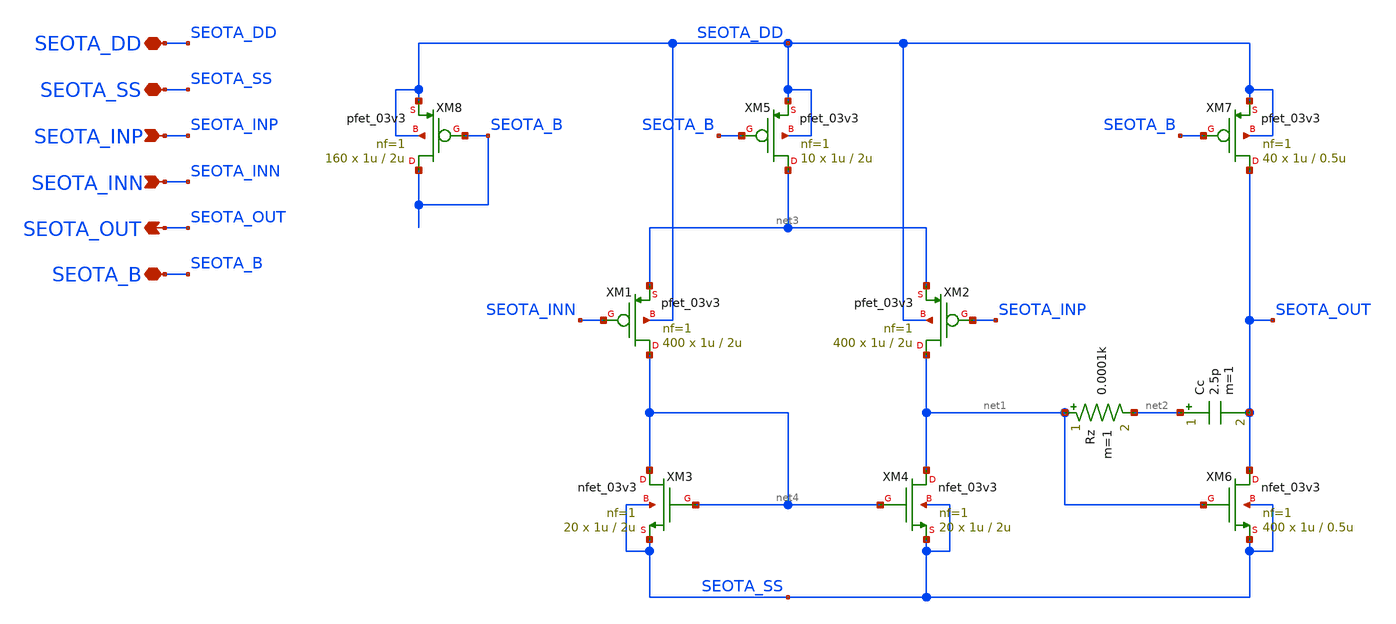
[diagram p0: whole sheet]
** sch_path: Design_Files/IC Design/Schematic/SE_OTA/SE_OTA_PMOS.sch
**.subckt SE_OTA_PMOS SEOTA_DD SEOTA_SS SEOTA_INP SEOTA_INN SEOTA_OUT SEOTA_B
*.iopin SEOTA_DD
*.iopin SEOTA_SS
*.ipin SEOTA_INP
*.ipin SEOTA_INN
*.opin SEOTA_OUT
*.iopin SEOTA_B
XM4 net1 net4 SEOTA_SS SEOTA_SS nfet_03v3 L=2u W=1u nf=1 ad='int((nf+1)/2) * W/nf * 0.18u' as='int((nf+2)/2) * W/nf * 0.18u'
+ pd='2*int((nf+1)/2) * (W/nf + 0.18u)' ps='2*int((nf+2)/2) * (W/nf + 0.18u)' nrd='0.18u / W' nrs='0.18u / W'
+ sa=0 sb=0 sd=0 m=20
XM3 net4 net4 SEOTA_SS SEOTA_SS nfet_03v3 L=2u W=1u nf=1 ad='int((nf+1)/2) * W/nf * 0.18u' as='int((nf+2)/2) * W/nf * 0.18u'
+ pd='2*int((nf+1)/2) * (W/nf + 0.18u)' ps='2*int((nf+2)/2) * (W/nf + 0.18u)' nrd='0.18u / W' nrs='0.18u / W'
+ sa=0 sb=0 sd=0 m=20
XM1 net4 SEOTA_INN net3 SEOTA_DD pfet_03v3 L=2u W=1u nf=1 ad='int((nf+1)/2) * W/nf * 0.18u' as='int((nf+2)/2) * W/nf * 0.18u'
+ pd='2*int((nf+1)/2) * (W/nf + 0.18u)' ps='2*int((nf+2)/2) * (W/nf + 0.18u)' nrd='0.18u / W' nrs='0.18u / W'
+ sa=0 sb=0 sd=0 m=400
XM2 net1 SEOTA_INP net3 SEOTA_DD pfet_03v3 L=2u W=1u nf=1 ad='int((nf+1)/2) * W/nf * 0.18u' as='int((nf+2)/2) * W/nf * 0.18u'
+ pd='2*int((nf+1)/2) * (W/nf + 0.18u)' ps='2*int((nf+2)/2) * (W/nf + 0.18u)' nrd='0.18u / W' nrs='0.18u / W'
+ sa=0 sb=0 sd=0 m=400
XM7 SEOTA_OUT SEOTA_B SEOTA_DD SEOTA_DD pfet_03v3 L=0.5u W=1u nf=1 ad='int((nf+1)/2) * W/nf * 0.18u'
+ as='int((nf+2)/2) * W/nf * 0.18u' pd='2*int((nf+1)/2) * (W/nf + 0.18u)' ps='2*int((nf+2)/2) * (W/nf + 0.18u)'
+ nrd='0.18u / W' nrs='0.18u / W' sa=0 sb=0 sd=0 m=40
Rz net1 net2 0.0001k m=1
XM5 net3 SEOTA_B SEOTA_DD SEOTA_DD pfet_03v3 L=2u W=1u nf=1 ad='int((nf+1)/2) * W/nf * 0.18u' as='int((nf+2)/2) * W/nf * 0.18u'
+ pd='2*int((nf+1)/2) * (W/nf + 0.18u)' ps='2*int((nf+2)/2) * (W/nf + 0.18u)' nrd='0.18u / W' nrs='0.18u / W'
+ sa=0 sb=0 sd=0 m=10
XM8 SEOTA_B SEOTA_B SEOTA_DD SEOTA_DD pfet_03v3 L=2u W=1u nf=1 ad='int((nf+1)/2) * W/nf * 0.18u' as='int((nf+2)/2) * W/nf * 0.18u'
+ pd='2*int((nf+1)/2) * (W/nf + 0.18u)' ps='2*int((nf+2)/2) * (W/nf + 0.18u)' nrd='0.18u / W' nrs='0.18u / W'
+ sa=0 sb=0 sd=0 m=160
Cc net2 SEOTA_OUT 2.5p m=1
XM6 SEOTA_OUT net1 SEOTA_SS SEOTA_SS nfet_03v3 L=0.5u W=1u nf=1 ad='int((nf+1)/2) * W/nf * 0.18u' as='int((nf+2)/2) * W/nf * 0.18u'
+ pd='2*int((nf+1)/2) * (W/nf + 0.18u)' ps='2*int((nf+2)/2) * (W/nf + 0.18u)' nrd='0.18u / W' nrs='0.18u / W'
+ sa=0 sb=0 sd=0 m=400
**.ends
.end
